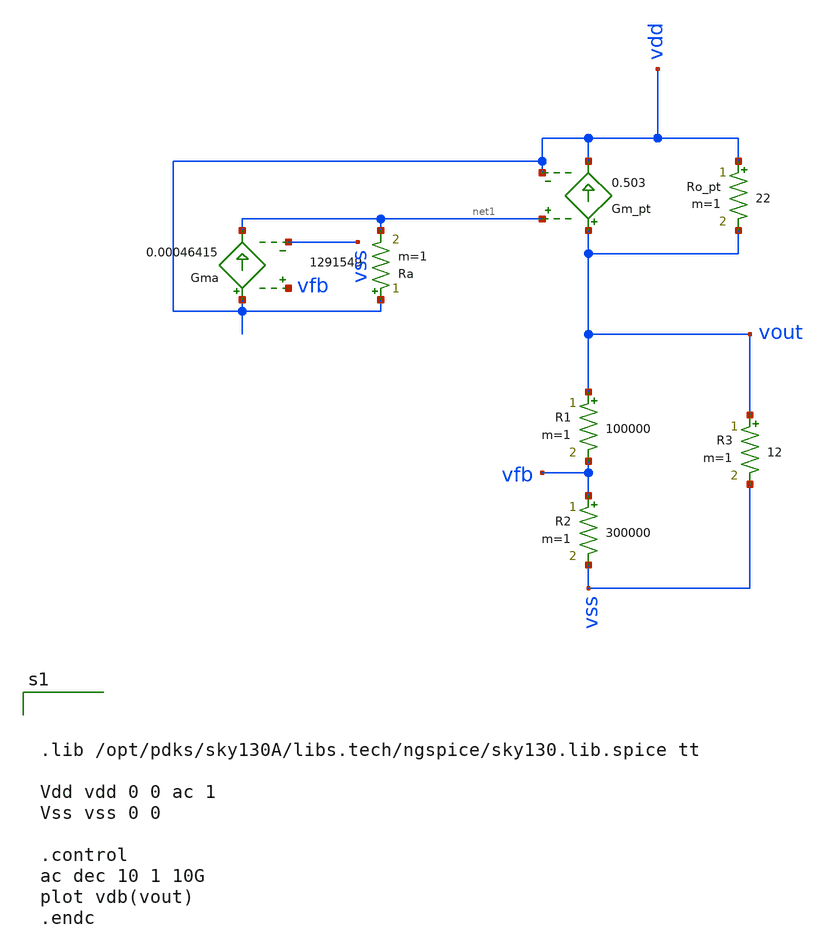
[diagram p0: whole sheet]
** sch_path: test/sstadex/xschem/ldo_tb.sch
**.subckt ldo_tb
Ro_pt vdd vout 22 m=1
Gm_pt vout vdd net1 vdd 0.503
R1 vout vfb 100000 m=1
R2 vfb vss 300000 m=1
R3 vout vss 12 m=1
Gma vdd net1 vfb vss 0.00046415
Ra vdd net1 1291549 m=1
**** begin user architecture code



.lib /opt/pdks/sky130A/libs.tech/ngspice/sky130.lib.spice tt

Vdd vdd 0 0 ac 1
Vss vss 0 0

.control
ac dec 10 1 10G
plot vdb(vout)
.endc



**** end user architecture code
**.ends
.end
